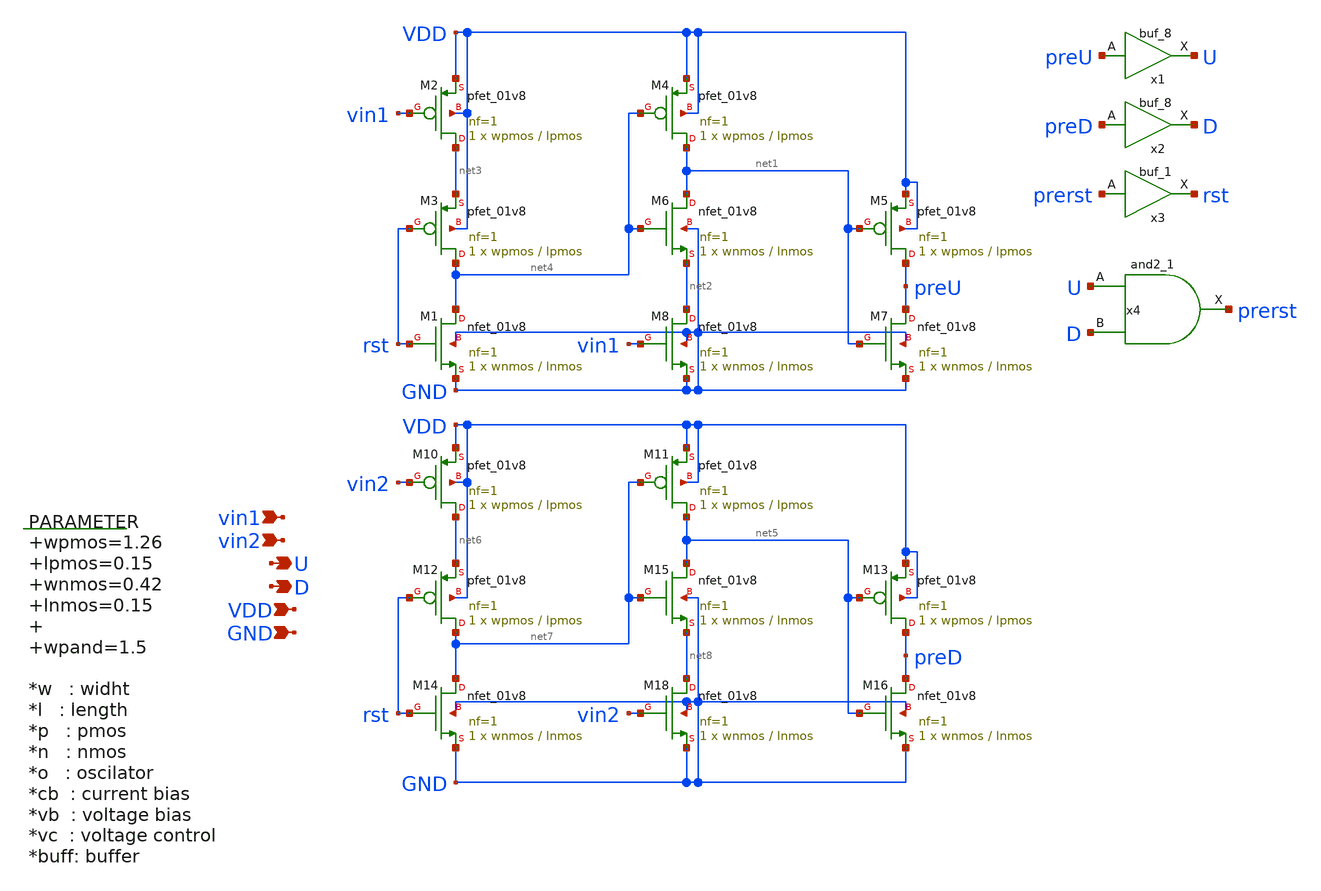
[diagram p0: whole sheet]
** sch_path: xschem/pfd.sch
**.subckt pfd vin1 vin2 U D VDD GND
*.ipin vin1
*.ipin vin2
*.opin U
*.opin D
*.ipin VDD
*.ipin GND
.param wpmos=1.26 lpmos=0.15 wnmos=0.42 lnmos=0.15 wpand=1.5

XM1 net4 rst GND GND sky130_fd_pr__nfet_01v8 L=lnmos W=wnmos nf=1 ad='int((nf+1)/2) * W/nf * 0.29' as='int((nf+2)/2) * W/nf * 0.29'
+ pd='2*int((nf+1)/2) * (W/nf + 0.29)' ps='2*int((nf+2)/2) * (W/nf + 0.29)' nrd='0.29 / W' nrs='0.29 / W'
+ sa=0 sb=0 sd=0 mult=1 m=1
XM2 net3 vin1 VDD VDD sky130_fd_pr__pfet_01v8 L=lpmos W=wpmos nf=1 ad='int((nf+1)/2) * W/nf * 0.29' as='int((nf+2)/2) * W/nf * 0.29'
+ pd='2*int((nf+1)/2) * (W/nf + 0.29)' ps='2*int((nf+2)/2) * (W/nf + 0.29)' nrd='0.29 / W' nrs='0.29 / W'
+ sa=0 sb=0 sd=0 mult=1 m=1
XM3 net4 rst net3 VDD sky130_fd_pr__pfet_01v8 L=lpmos W=wpmos nf=1 ad='int((nf+1)/2) * W/nf * 0.29' as='int((nf+2)/2) * W/nf * 0.29'
+ pd='2*int((nf+1)/2) * (W/nf + 0.29)' ps='2*int((nf+2)/2) * (W/nf + 0.29)' nrd='0.29 / W' nrs='0.29 / W'
+ sa=0 sb=0 sd=0 mult=1 m=1
XM4 net1 net4 VDD VDD sky130_fd_pr__pfet_01v8 L=lpmos W=wpmos nf=1 ad='int((nf+1)/2) * W/nf * 0.29' as='int((nf+2)/2) * W/nf * 0.29'
+ pd='2*int((nf+1)/2) * (W/nf + 0.29)' ps='2*int((nf+2)/2) * (W/nf + 0.29)' nrd='0.29 / W' nrs='0.29 / W'
+ sa=0 sb=0 sd=0 mult=1 m=1
XM5 preU net1 VDD VDD sky130_fd_pr__pfet_01v8 L=lpmos W=wpmos nf=1 ad='int((nf+1)/2) * W/nf * 0.29' as='int((nf+2)/2) * W/nf * 0.29'
+ pd='2*int((nf+1)/2) * (W/nf + 0.29)' ps='2*int((nf+2)/2) * (W/nf + 0.29)' nrd='0.29 / W' nrs='0.29 / W'
+ sa=0 sb=0 sd=0 mult=1 m=1
XM6 net1 net4 net2 GND sky130_fd_pr__nfet_01v8 L=lnmos W=wnmos nf=1 ad='int((nf+1)/2) * W/nf * 0.29'
+ as='int((nf+2)/2) * W/nf * 0.29' pd='2*int((nf+1)/2) * (W/nf + 0.29)' ps='2*int((nf+2)/2) * (W/nf + 0.29)'
+ nrd='0.29 / W' nrs='0.29 / W' sa=0 sb=0 sd=0 mult=1 m=1
XM7 preU net1 GND GND sky130_fd_pr__nfet_01v8 L=lnmos W=wnmos nf=1 ad='int((nf+1)/2) * W/nf * 0.29' as='int((nf+2)/2) * W/nf * 0.29'
+ pd='2*int((nf+1)/2) * (W/nf + 0.29)' ps='2*int((nf+2)/2) * (W/nf + 0.29)' nrd='0.29 / W' nrs='0.29 / W'
+ sa=0 sb=0 sd=0 mult=1 m=1
XM8 net2 vin1 GND GND sky130_fd_pr__nfet_01v8 L=lnmos W=wnmos nf=1 ad='int((nf+1)/2) * W/nf * 0.29' as='int((nf+2)/2) * W/nf * 0.29'
+ pd='2*int((nf+1)/2) * (W/nf + 0.29)' ps='2*int((nf+2)/2) * (W/nf + 0.29)' nrd='0.29 / W' nrs='0.29 / W'
+ sa=0 sb=0 sd=0 mult=1 m=1
XM10 net6 vin2 VDD VDD sky130_fd_pr__pfet_01v8 L=lpmos W=wpmos nf=1 ad='int((nf+1)/2) * W/nf * 0.29'
+ as='int((nf+2)/2) * W/nf * 0.29' pd='2*int((nf+1)/2) * (W/nf + 0.29)' ps='2*int((nf+2)/2) * (W/nf + 0.29)'
+ nrd='0.29 / W' nrs='0.29 / W' sa=0 sb=0 sd=0 mult=1 m=1
XM11 net5 net7 VDD VDD sky130_fd_pr__pfet_01v8 L=lpmos W=wpmos nf=1 ad='int((nf+1)/2) * W/nf * 0.29'
+ as='int((nf+2)/2) * W/nf * 0.29' pd='2*int((nf+1)/2) * (W/nf + 0.29)' ps='2*int((nf+2)/2) * (W/nf + 0.29)'
+ nrd='0.29 / W' nrs='0.29 / W' sa=0 sb=0 sd=0 mult=1 m=1
XM12 net7 rst net6 VDD sky130_fd_pr__pfet_01v8 L=lpmos W=wpmos nf=1 ad='int((nf+1)/2) * W/nf * 0.29'
+ as='int((nf+2)/2) * W/nf * 0.29' pd='2*int((nf+1)/2) * (W/nf + 0.29)' ps='2*int((nf+2)/2) * (W/nf + 0.29)'
+ nrd='0.29 / W' nrs='0.29 / W' sa=0 sb=0 sd=0 mult=1 m=1
XM13 preD net5 VDD VDD sky130_fd_pr__pfet_01v8 L=lpmos W=wpmos nf=1 ad='int((nf+1)/2) * W/nf * 0.29'
+ as='int((nf+2)/2) * W/nf * 0.29' pd='2*int((nf+1)/2) * (W/nf + 0.29)' ps='2*int((nf+2)/2) * (W/nf + 0.29)'
+ nrd='0.29 / W' nrs='0.29 / W' sa=0 sb=0 sd=0 mult=1 m=1
XM14 net7 rst GND GND sky130_fd_pr__nfet_01v8 L=lnmos W=wnmos nf=1 ad='int((nf+1)/2) * W/nf * 0.29' as='int((nf+2)/2) * W/nf * 0.29'
+ pd='2*int((nf+1)/2) * (W/nf + 0.29)' ps='2*int((nf+2)/2) * (W/nf + 0.29)' nrd='0.29 / W' nrs='0.29 / W'
+ sa=0 sb=0 sd=0 mult=1 m=1
XM15 net5 net7 net8 GND sky130_fd_pr__nfet_01v8 L=lnmos W=wnmos nf=1 ad='int((nf+1)/2) * W/nf * 0.29'
+ as='int((nf+2)/2) * W/nf * 0.29' pd='2*int((nf+1)/2) * (W/nf + 0.29)' ps='2*int((nf+2)/2) * (W/nf + 0.29)'
+ nrd='0.29 / W' nrs='0.29 / W' sa=0 sb=0 sd=0 mult=1 m=1
XM16 preD net5 GND GND sky130_fd_pr__nfet_01v8 L=lnmos W=wnmos nf=1 ad='int((nf+1)/2) * W/nf * 0.29'
+ as='int((nf+2)/2) * W/nf * 0.29' pd='2*int((nf+1)/2) * (W/nf + 0.29)' ps='2*int((nf+2)/2) * (W/nf + 0.29)'
+ nrd='0.29 / W' nrs='0.29 / W' sa=0 sb=0 sd=0 mult=1 m=1
XM18 net8 vin2 GND GND sky130_fd_pr__nfet_01v8 L=lnmos W=wnmos nf=1 ad='int((nf+1)/2) * W/nf * 0.29'
+ as='int((nf+2)/2) * W/nf * 0.29' pd='2*int((nf+1)/2) * (W/nf + 0.29)' ps='2*int((nf+2)/2) * (W/nf + 0.29)'
+ nrd='0.29 / W' nrs='0.29 / W' sa=0 sb=0 sd=0 mult=1 m=1
x1 preU GND GND VDD VDD U sky130_fd_sc_hd__buf_8
x2 preD GND GND VDD VDD D sky130_fd_sc_hd__buf_8
x3 prerst GND GND VDD VDD rst sky130_fd_sc_hd__buf_1
x4 U D GND GND VDD VDD prerst sky130_fd_sc_hd__and2_1
**.ends
.end
